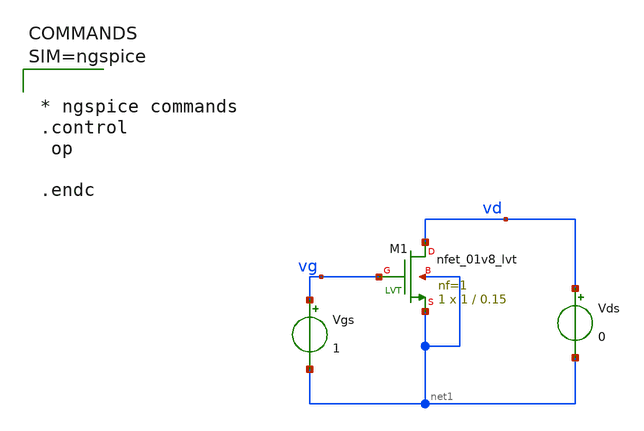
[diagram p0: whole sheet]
** sch_path: xschem/untitled.sch
**.subckt untitled
XM1 vd vg net1 net1 sky130_fd_pr__nfet_01v8_lvt L=0.15 W=1 nf=1 ad='int((1 + 1)/2) * 1 / 1 * 0.29' as='int((1 + 2)/2) * 1 / 1 * 0.29'
+ pd='2*int((1 + 1)/2) * (1 / 1 + 0.29)' ps='2*int((1 + 2)/2) * (1 / 1 + 0.29)' nrd='0.29 / 1 ' nrs='0.29 / 1 '
+ sa=0 sb=0 sd=0 mult=1 m=1
Vgs vg net1 1
Vds vd net1 0
**** begin user architecture code

** opencircuitdesign pdks install
.lib $::SKYWATER_MODELS/sky130.lib.spice tt




* ngspice commands
.control
 op

.endc



**** end user architecture code
**.ends
.end
